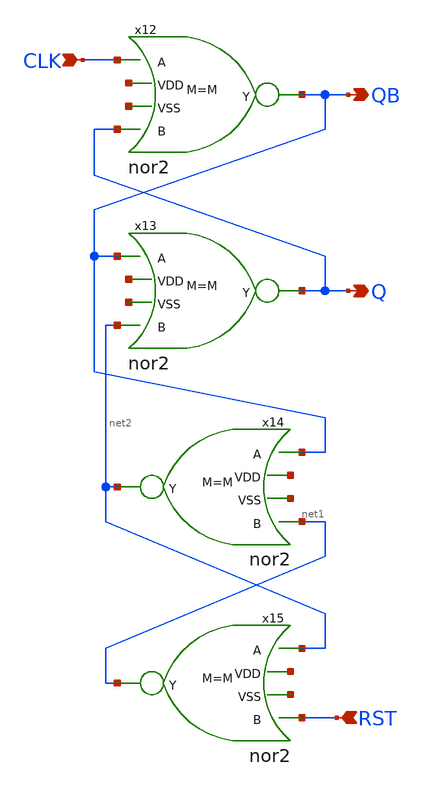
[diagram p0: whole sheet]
** sch_path: designs/pfd_latch.sch
**.subckt pfd_latch CLK Q QB RST
*.ipin CLK
*.opin Q
*.opin QB
*.ipin RST
x12 CLK QB Q net3 net4 nor2 M=M
x13 QB Q net2 net5 net6 nor2 M=M
x14 QB net2 net1 net7 net8 nor2 M=M
x15 net2 net1 RST net9 net10 nor2 M=M
**.ends

* expanding   symbol:
*+  /home/users/nhpoole/ee272b/ee272b_mixed_signal_mmwave_accelerator/designs/nor2.sym # of pins=5
** sym_path: designs/nor2.sym
** sch_path: designs/nor2.sch
.subckt nor2 A Y B VDD VSS  M=1
*.ipin A
*.ipin B
*.opin Y
*.ipin VDD
*.ipin VSS
XM2 Y A VSS VSS sky130_fd_pr__nfet_01v8 L=0.15 W=0.65 nf=1 ad='int((nf+1)/2) * W/nf * 0.29' as='int((nf+2)/2) * W/nf * 0.29'
+ pd='2*int((nf+1)/2) * (W/nf + 0.29)' ps='2*int((nf+2)/2) * (W/nf + 0.29)' nrd='0.29 / W' nrs='0.29 / W'
+ sa=0 sb=0 sd=0 mult=M m=M
XM1 net1 A VDD VDD sky130_fd_pr__pfet_01v8_hvt L=0.15 W=1 nf=1 ad='int((nf+1)/2) * W/nf * 0.29' as='int((nf+2)/2) * W/nf * 0.29'
+ pd='2*int((nf+1)/2) * (W/nf + 0.29)' ps='2*int((nf+2)/2) * (W/nf + 0.29)' nrd='0.29 / W' nrs='0.29 / W'
+ sa=0 sb=0 sd=0 mult=M m=M
XM3 Y B VSS VSS sky130_fd_pr__nfet_01v8 L=0.15 W=0.65 nf=1 ad='int((nf+1)/2) * W/nf * 0.29' as='int((nf+2)/2) * W/nf * 0.29'
+ pd='2*int((nf+1)/2) * (W/nf + 0.29)' ps='2*int((nf+2)/2) * (W/nf + 0.29)' nrd='0.29 / W' nrs='0.29 / W'
+ sa=0 sb=0 sd=0 mult=M m=M
XM4 Y B net1 VDD sky130_fd_pr__pfet_01v8_hvt L=0.15 W=1 nf=1 ad='int((nf+1)/2) * W/nf * 0.29' as='int((nf+2)/2) * W/nf * 0.29'
+ pd='2*int((nf+1)/2) * (W/nf + 0.29)' ps='2*int((nf+2)/2) * (W/nf + 0.29)' nrd='0.29 / W' nrs='0.29 / W'
+ sa=0 sb=0 sd=0 mult=M m=M
.ends

.end
